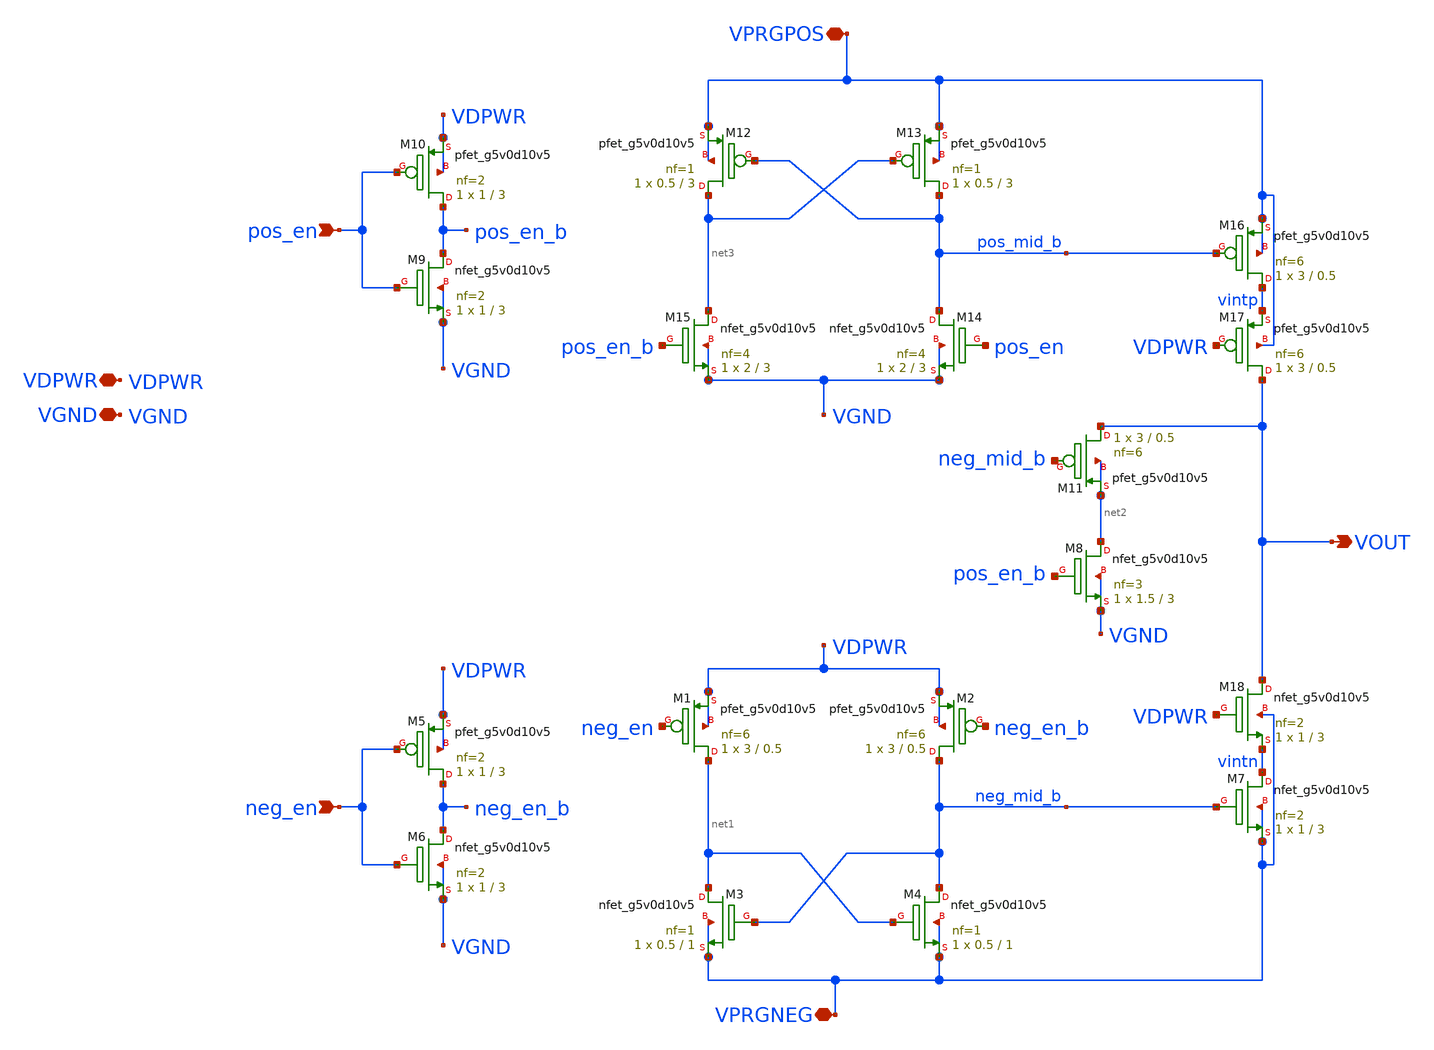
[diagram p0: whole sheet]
** sch_path: xschem/vprog_controller.sch
**.subckt vprog_controller VPRGNEG neg_en VOUT VDPWR pos_en VGND VPRGPOS
*.iopin VPRGNEG
*.ipin neg_en
*.opin VOUT
*.iopin VDPWR
*.ipin pos_en
*.iopin VGND
*.iopin VPRGPOS
XM1 net1 neg_en VDPWR VDPWR sky130_fd_pr__pfet_g5v0d10v5 L=0.5 W=3 nf=6 ad='int((nf+1)/2) * W/nf * 0.29'
+ as='int((nf+2)/2) * W/nf * 0.29' pd='2*int((nf+1)/2) * (W/nf + 0.29)' ps='2*int((nf+2)/2) * (W/nf + 0.29)'
+ nrd='0.29 / W' nrs='0.29 / W' sa=0 sb=0 sd=0 mult=1 m=1
XM2 neg_mid_b neg_en_b VDPWR VDPWR sky130_fd_pr__pfet_g5v0d10v5 L=0.5 W=3 nf=6 ad='int((nf+1)/2) * W/nf * 0.29'
+ as='int((nf+2)/2) * W/nf * 0.29' pd='2*int((nf+1)/2) * (W/nf + 0.29)' ps='2*int((nf+2)/2) * (W/nf + 0.29)'
+ nrd='0.29 / W' nrs='0.29 / W' sa=0 sb=0 sd=0 mult=1 m=1
XM4 neg_mid_b net1 VPRGNEG VPRGNEG sky130_fd_pr__nfet_g5v0d10v5 L=1 W=0.5 nf=1 ad='int((nf+1)/2) * W/nf * 0.29'
+ as='int((nf+2)/2) * W/nf * 0.29' pd='2*int((nf+1)/2) * (W/nf + 0.29)' ps='2*int((nf+2)/2) * (W/nf + 0.29)'
+ nrd='0.29 / W' nrs='0.29 / W' sa=0 sb=0 sd=0 mult=1 m=1
XM3 net1 neg_mid_b VPRGNEG VPRGNEG sky130_fd_pr__nfet_g5v0d10v5 L=1 W=0.5 nf=1 ad='int((nf+1)/2) * W/nf * 0.29'
+ as='int((nf+2)/2) * W/nf * 0.29' pd='2*int((nf+1)/2) * (W/nf + 0.29)' ps='2*int((nf+2)/2) * (W/nf + 0.29)'
+ nrd='0.29 / W' nrs='0.29 / W' sa=0 sb=0 sd=0 mult=1 m=1
XM7 vintn neg_mid_b VPRGNEG VPRGNEG sky130_fd_pr__nfet_g5v0d10v5 L=3 W=1 nf=2 ad='int((nf+1)/2) * W/nf * 0.29'
+ as='int((nf+2)/2) * W/nf * 0.29' pd='2*int((nf+1)/2) * (W/nf + 0.29)' ps='2*int((nf+2)/2) * (W/nf + 0.29)'
+ nrd='0.29 / W' nrs='0.29 / W' sa=0 sb=0 sd=0 mult=1 m=1
XM8 net2 pos_en_b VGND VGND sky130_fd_pr__nfet_g5v0d10v5 L=3 W=1.5 nf=3 ad='int((nf+1)/2) * W/nf * 0.29'
+ as='int((nf+2)/2) * W/nf * 0.29' pd='2*int((nf+1)/2) * (W/nf + 0.29)' ps='2*int((nf+2)/2) * (W/nf + 0.29)'
+ nrd='0.29 / W' nrs='0.29 / W' sa=0 sb=0 sd=0 mult=1 m=1
XM12 net3 pos_mid_b VPRGPOS VPRGPOS sky130_fd_pr__pfet_g5v0d10v5 L=3 W=0.5 nf=1 ad='int((nf+1)/2) * W/nf * 0.29'
+ as='int((nf+2)/2) * W/nf * 0.29' pd='2*int((nf+1)/2) * (W/nf + 0.29)' ps='2*int((nf+2)/2) * (W/nf + 0.29)'
+ nrd='0.29 / W' nrs='0.29 / W' sa=0 sb=0 sd=0 mult=1 m=1
XM13 pos_mid_b net3 VPRGPOS VPRGPOS sky130_fd_pr__pfet_g5v0d10v5 L=3 W=0.5 nf=1 ad='int((nf+1)/2) * W/nf * 0.29'
+ as='int((nf+2)/2) * W/nf * 0.29' pd='2*int((nf+1)/2) * (W/nf + 0.29)' ps='2*int((nf+2)/2) * (W/nf + 0.29)'
+ nrd='0.29 / W' nrs='0.29 / W' sa=0 sb=0 sd=0 mult=1 m=1
XM14 pos_mid_b pos_en VGND VGND sky130_fd_pr__nfet_g5v0d10v5 L=3 W=2 nf=4 ad='int((nf+1)/2) * W/nf * 0.29'
+ as='int((nf+2)/2) * W/nf * 0.29' pd='2*int((nf+1)/2) * (W/nf + 0.29)' ps='2*int((nf+2)/2) * (W/nf + 0.29)'
+ nrd='0.29 / W' nrs='0.29 / W' sa=0 sb=0 sd=0 mult=1 m=1
XM15 net3 pos_en_b VGND VGND sky130_fd_pr__nfet_g5v0d10v5 L=3 W=2 nf=4 ad='int((nf+1)/2) * W/nf * 0.29'
+ as='int((nf+2)/2) * W/nf * 0.29' pd='2*int((nf+1)/2) * (W/nf + 0.29)' ps='2*int((nf+2)/2) * (W/nf + 0.29)'
+ nrd='0.29 / W' nrs='0.29 / W' sa=0 sb=0 sd=0 mult=1 m=1
XM16 vintp pos_mid_b VPRGPOS VPRGPOS sky130_fd_pr__pfet_g5v0d10v5 L=0.5 W=3 nf=6 ad='int((nf+1)/2) * W/nf * 0.29'
+ as='int((nf+2)/2) * W/nf * 0.29' pd='2*int((nf+1)/2) * (W/nf + 0.29)' ps='2*int((nf+2)/2) * (W/nf + 0.29)'
+ nrd='0.29 / W' nrs='0.29 / W' sa=0 sb=0 sd=0 mult=1 m=1
XM11 VOUT neg_mid_b net2 net2 sky130_fd_pr__pfet_g5v0d10v5 L=0.5 W=3 nf=6 ad='int((nf+1)/2) * W/nf * 0.29'
+ as='int((nf+2)/2) * W/nf * 0.29' pd='2*int((nf+1)/2) * (W/nf + 0.29)' ps='2*int((nf+2)/2) * (W/nf + 0.29)'
+ nrd='0.29 / W' nrs='0.29 / W' sa=0 sb=0 sd=0 mult=1 m=1
XM17 VOUT VDPWR vintp VPRGPOS sky130_fd_pr__pfet_g5v0d10v5 L=0.5 W=3 nf=6 ad='int((nf+1)/2) * W/nf * 0.29'
+ as='int((nf+2)/2) * W/nf * 0.29' pd='2*int((nf+1)/2) * (W/nf + 0.29)' ps='2*int((nf+2)/2) * (W/nf + 0.29)'
+ nrd='0.29 / W' nrs='0.29 / W' sa=0 sb=0 sd=0 mult=1 m=1
XM18 VOUT VDPWR vintn VPRGNEG sky130_fd_pr__nfet_g5v0d10v5 L=3 W=1 nf=2 ad='int((nf+1)/2) * W/nf * 0.29'
+ as='int((nf+2)/2) * W/nf * 0.29' pd='2*int((nf+1)/2) * (W/nf + 0.29)' ps='2*int((nf+2)/2) * (W/nf + 0.29)'
+ nrd='0.29 / W' nrs='0.29 / W' sa=0 sb=0 sd=0 mult=1 m=1
XM5 neg_en_b neg_en VDPWR VDPWR sky130_fd_pr__pfet_g5v0d10v5 L=3 W=1 nf=2 ad='int((nf+1)/2) * W/nf * 0.29'
+ as='int((nf+2)/2) * W/nf * 0.29' pd='2*int((nf+1)/2) * (W/nf + 0.29)' ps='2*int((nf+2)/2) * (W/nf + 0.29)'
+ nrd='0.29 / W' nrs='0.29 / W' sa=0 sb=0 sd=0 mult=1 m=1
XM6 neg_en_b neg_en VGND VGND sky130_fd_pr__nfet_g5v0d10v5 L=3 W=1 nf=2 ad='int((nf+1)/2) * W/nf * 0.29'
+ as='int((nf+2)/2) * W/nf * 0.29' pd='2*int((nf+1)/2) * (W/nf + 0.29)' ps='2*int((nf+2)/2) * (W/nf + 0.29)'
+ nrd='0.29 / W' nrs='0.29 / W' sa=0 sb=0 sd=0 mult=1 m=1
XM9 pos_en_b pos_en VGND VGND sky130_fd_pr__nfet_g5v0d10v5 L=3 W=1 nf=2 ad='int((nf+1)/2) * W/nf * 0.29'
+ as='int((nf+2)/2) * W/nf * 0.29' pd='2*int((nf+1)/2) * (W/nf + 0.29)' ps='2*int((nf+2)/2) * (W/nf + 0.29)'
+ nrd='0.29 / W' nrs='0.29 / W' sa=0 sb=0 sd=0 mult=1 m=1
XM10 pos_en_b pos_en VDPWR VDPWR sky130_fd_pr__pfet_g5v0d10v5 L=3 W=1 nf=2 ad='int((nf+1)/2) * W/nf * 0.29'
+ as='int((nf+2)/2) * W/nf * 0.29' pd='2*int((nf+1)/2) * (W/nf + 0.29)' ps='2*int((nf+2)/2) * (W/nf + 0.29)'
+ nrd='0.29 / W' nrs='0.29 / W' sa=0 sb=0 sd=0 mult=1 m=1
**.ends
.end
